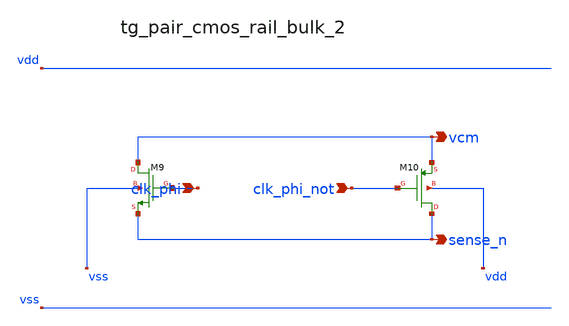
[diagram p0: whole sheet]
** sch_path: analog-db/raw/cmfb_004_output_switched_cap/hier/blocks/tg_pair_cmos_rail_bulk_2.sch
**.subckt tg_pair_cmos_rail_bulk_2 clk_phi clk_phi_not vcm sense_n
*.ipin clk_phi
*.ipin clk_phi_not
*.opin vcm
*.opin sense_n
XM10 sense_n clk_phi_not vcm vdd sg13_lv_pmos w=x_dut_xm10_w l=x_dut_xm10_l ng=1 m=x_dut_xm10_m
XM9 vcm clk_phi sense_n vss sg13_lv_nmos w=x_dut_xm9_w l=x_dut_xm9_l ng=1 m=x_dut_xm9_m
**.ends
.end
